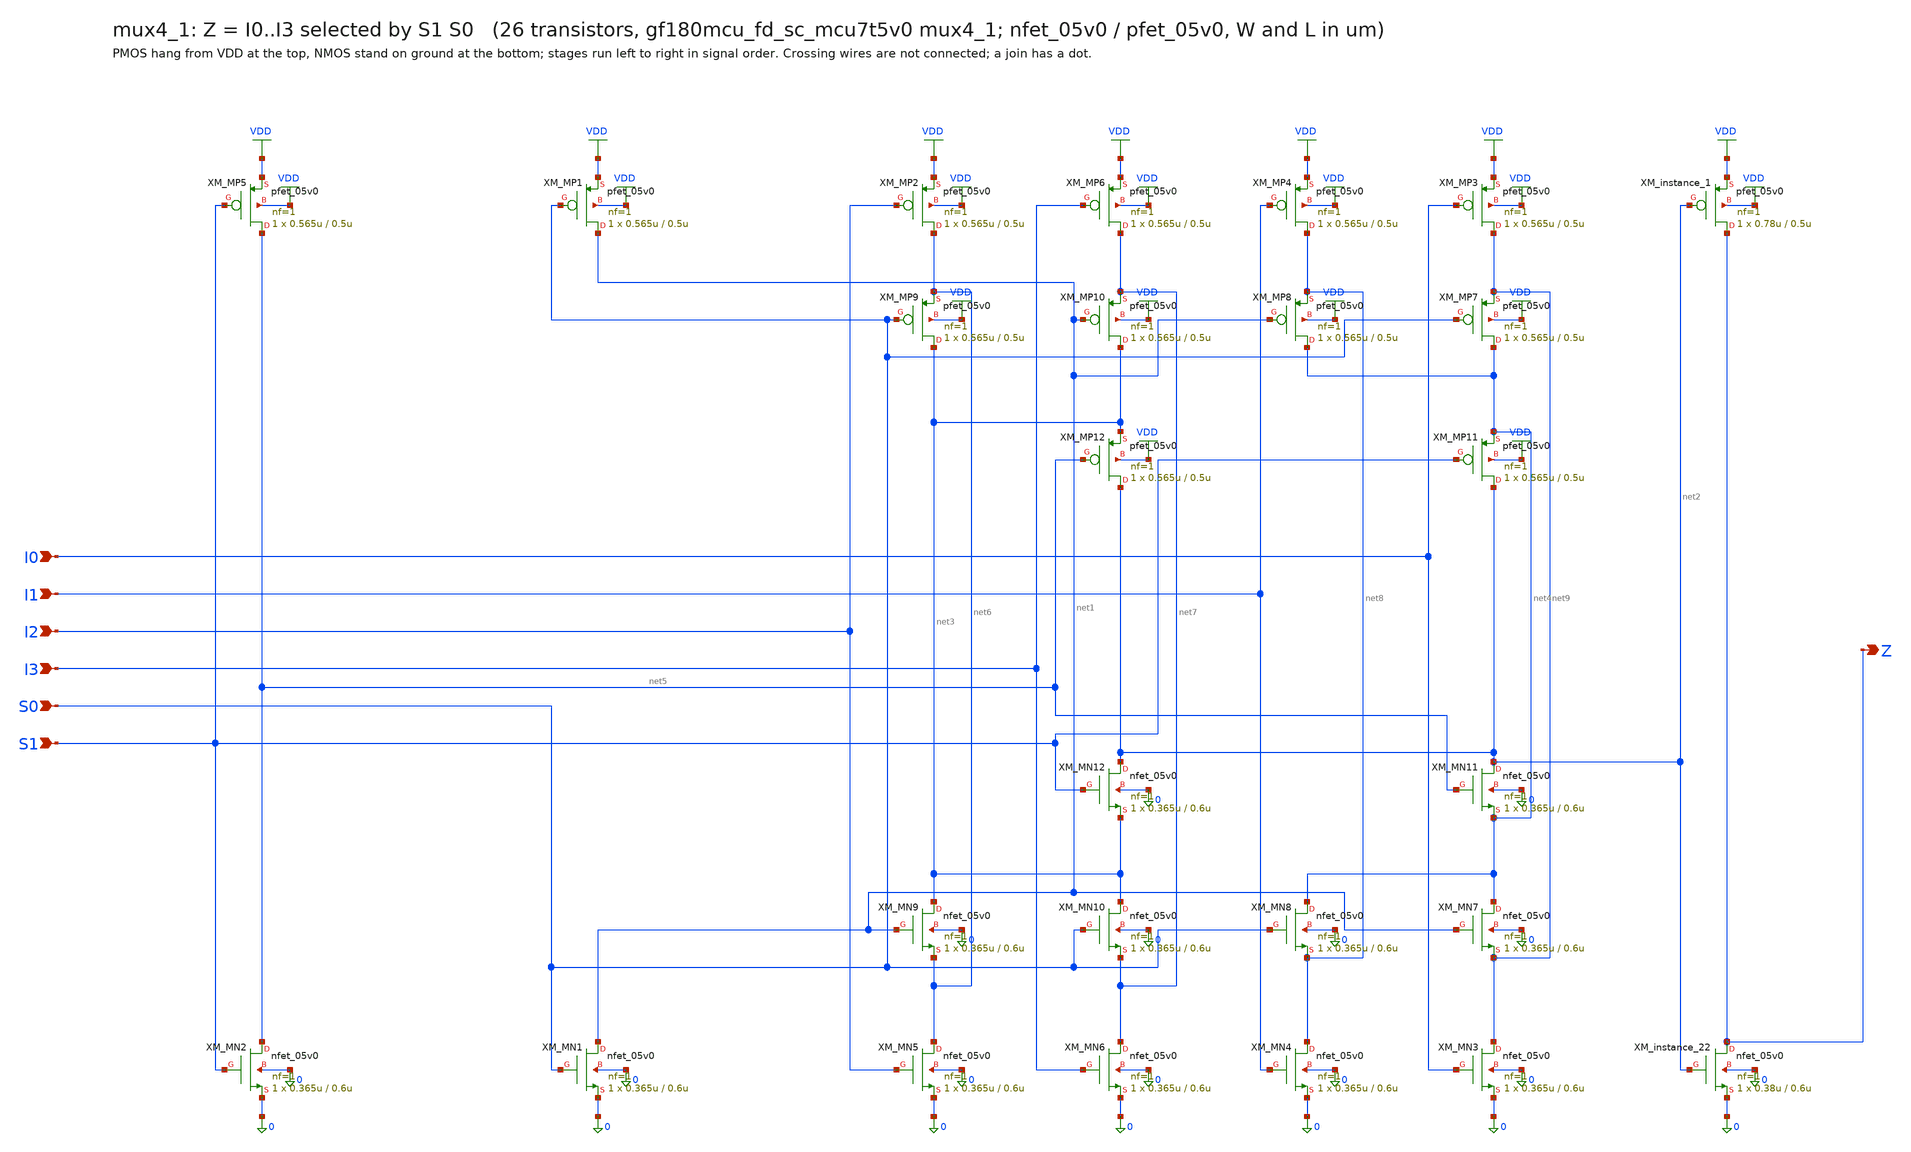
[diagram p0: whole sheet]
** sch_path: xschem/cells_tx/mux4_1.sch
**.subckt mux4_1 I0 I1 I2 I3 S0 S1 Z
*.ipin I0
*.ipin I1
*.ipin I2
*.ipin I3
*.ipin S0
*.ipin S1
*.opin Z
XM_MN5 net6 I2 0 0 nfet_05v0 L=0.6u W=0.365u nf=1 ad=1.825e-13 as=1.825e-13 pd=1.73e-06 ps=1.73e-06
+ nrd=0 nrs=0 sa=0 sb=0 sd=0 m=1
XM_MN9 net3 net1 net6 0 nfet_05v0 L=0.6u W=0.365u nf=1 ad=1.825e-13 as=1.825e-13 pd=1.73e-06
+ ps=1.73e-06 nrd=0 nrs=0 sa=0 sb=0 sd=0 m=1
XM_MN10 net3 S0 net7 0 nfet_05v0 L=0.6u W=0.365u nf=1 ad=1.825e-13 as=1.825e-13 pd=1.73e-06
+ ps=1.73e-06 nrd=0 nrs=0 sa=0 sb=0 sd=0 m=1
XM_MN6 net7 I3 0 0 nfet_05v0 L=0.6u W=0.365u nf=1 ad=1.825e-13 as=1.825e-13 pd=1.73e-06 ps=1.73e-06
+ nrd=0 nrs=0 sa=0 sb=0 sd=0 m=1
XM_instance_22 Z net2 0 0 nfet_05v0 L=0.6u W=0.38u nf=1 ad=1.9e-13 as=1.9e-13 pd=1.76e-06
+ ps=1.76e-06 nrd=0 nrs=0 sa=0 sb=0 sd=0 m=1
XM_MN12 net2 S1 net3 0 nfet_05v0 L=0.6u W=0.365u nf=1 ad=1.825e-13 as=1.825e-13 pd=1.73e-06
+ ps=1.73e-06 nrd=0 nrs=0 sa=0 sb=0 sd=0 m=1
XM_MN11 net2 net5 net4 0 nfet_05v0 L=0.6u W=0.365u nf=1 ad=1.825e-13 as=1.825e-13 pd=1.73e-06
+ ps=1.73e-06 nrd=0 nrs=0 sa=0 sb=0 sd=0 m=1
XM_MN2 net5 S1 0 0 nfet_05v0 L=0.6u W=0.365u nf=1 ad=1.825e-13 as=1.825e-13 pd=1.73e-06 ps=1.73e-06
+ nrd=0 nrs=0 sa=0 sb=0 sd=0 m=1
XM_MN4 net8 I1 0 0 nfet_05v0 L=0.6u W=0.365u nf=1 ad=1.825e-13 as=1.825e-13 pd=1.73e-06 ps=1.73e-06
+ nrd=0 nrs=0 sa=0 sb=0 sd=0 m=1
XM_MN8 net4 S0 net8 0 nfet_05v0 L=0.6u W=0.365u nf=1 ad=1.825e-13 as=1.825e-13 pd=1.73e-06
+ ps=1.73e-06 nrd=0 nrs=0 sa=0 sb=0 sd=0 m=1
XM_MN7 net4 net1 net9 0 nfet_05v0 L=0.6u W=0.365u nf=1 ad=1.825e-13 as=1.825e-13 pd=1.73e-06
+ ps=1.73e-06 nrd=0 nrs=0 sa=0 sb=0 sd=0 m=1
XM_MN3 net9 I0 0 0 nfet_05v0 L=0.6u W=0.365u nf=1 ad=1.825e-13 as=1.825e-13 pd=1.73e-06 ps=1.73e-06
+ nrd=0 nrs=0 sa=0 sb=0 sd=0 m=1
XM_MN1 net1 S0 0 0 nfet_05v0 L=0.6u W=0.365u nf=1 ad=1.825e-13 as=1.825e-13 pd=1.73e-06 ps=1.73e-06
+ nrd=0 nrs=0 sa=0 sb=0 sd=0 m=1
XM_MP2 net6 I2 VDD VDD pfet_05v0 L=0.5u W=0.565u nf=1 ad=2.825e-13 as=2.825e-13 pd=2.13e-06
+ ps=2.13e-06 nrd=0 nrs=0 sa=0 sb=0 sd=0 m=1
XM_MP9 net3 S0 net6 VDD pfet_05v0 L=0.5u W=0.565u nf=1 ad=2.825e-13 as=2.825e-13 pd=2.13e-06
+ ps=2.13e-06 nrd=0 nrs=0 sa=0 sb=0 sd=0 m=1
XM_MP10 net3 net1 net7 VDD pfet_05v0 L=0.5u W=0.565u nf=1 ad=2.825e-13 as=2.825e-13 pd=2.13e-06
+ ps=2.13e-06 nrd=0 nrs=0 sa=0 sb=0 sd=0 m=1
XM_MP6 net7 I3 VDD VDD pfet_05v0 L=0.5u W=0.565u nf=1 ad=2.825e-13 as=2.825e-13 pd=2.13e-06
+ ps=2.13e-06 nrd=0 nrs=0 sa=0 sb=0 sd=0 m=1
XM_instance_1 Z net2 VDD VDD pfet_05v0 L=0.5u W=0.78u nf=1 ad=3.9e-13 as=3.9e-13 pd=2.56e-06
+ ps=2.56e-06 nrd=0 nrs=0 sa=0 sb=0 sd=0 m=1
XM_MP12 net2 net5 net3 VDD pfet_05v0 L=0.5u W=0.565u nf=1 ad=2.825e-13 as=2.825e-13 pd=2.13e-06
+ ps=2.13e-06 nrd=0 nrs=0 sa=0 sb=0 sd=0 m=1
XM_MP11 net2 S1 net4 VDD pfet_05v0 L=0.5u W=0.565u nf=1 ad=2.825e-13 as=2.825e-13 pd=2.13e-06
+ ps=2.13e-06 nrd=0 nrs=0 sa=0 sb=0 sd=0 m=1
XM_MP5 net5 S1 VDD VDD pfet_05v0 L=0.5u W=0.565u nf=1 ad=2.825e-13 as=2.825e-13 pd=2.13e-06
+ ps=2.13e-06 nrd=0 nrs=0 sa=0 sb=0 sd=0 m=1
XM_MP4 net8 I1 VDD VDD pfet_05v0 L=0.5u W=0.565u nf=1 ad=2.825e-13 as=2.825e-13 pd=2.13e-06
+ ps=2.13e-06 nrd=0 nrs=0 sa=0 sb=0 sd=0 m=1
XM_MP8 net4 net1 net8 VDD pfet_05v0 L=0.5u W=0.565u nf=1 ad=2.825e-13 as=2.825e-13 pd=2.13e-06
+ ps=2.13e-06 nrd=0 nrs=0 sa=0 sb=0 sd=0 m=1
XM_MP7 net4 S0 net9 VDD pfet_05v0 L=0.5u W=0.565u nf=1 ad=2.825e-13 as=2.825e-13 pd=2.13e-06
+ ps=2.13e-06 nrd=0 nrs=0 sa=0 sb=0 sd=0 m=1
XM_MP3 net9 I0 VDD VDD pfet_05v0 L=0.5u W=0.565u nf=1 ad=2.825e-13 as=2.825e-13 pd=2.13e-06
+ ps=2.13e-06 nrd=0 nrs=0 sa=0 sb=0 sd=0 m=1
XM_MP1 net1 S0 VDD VDD pfet_05v0 L=0.5u W=0.565u nf=1 ad=2.825e-13 as=2.825e-13 pd=2.13e-06
+ ps=2.13e-06 nrd=0 nrs=0 sa=0 sb=0 sd=0 m=1
**.ends
.GLOBAL VDD
.end
